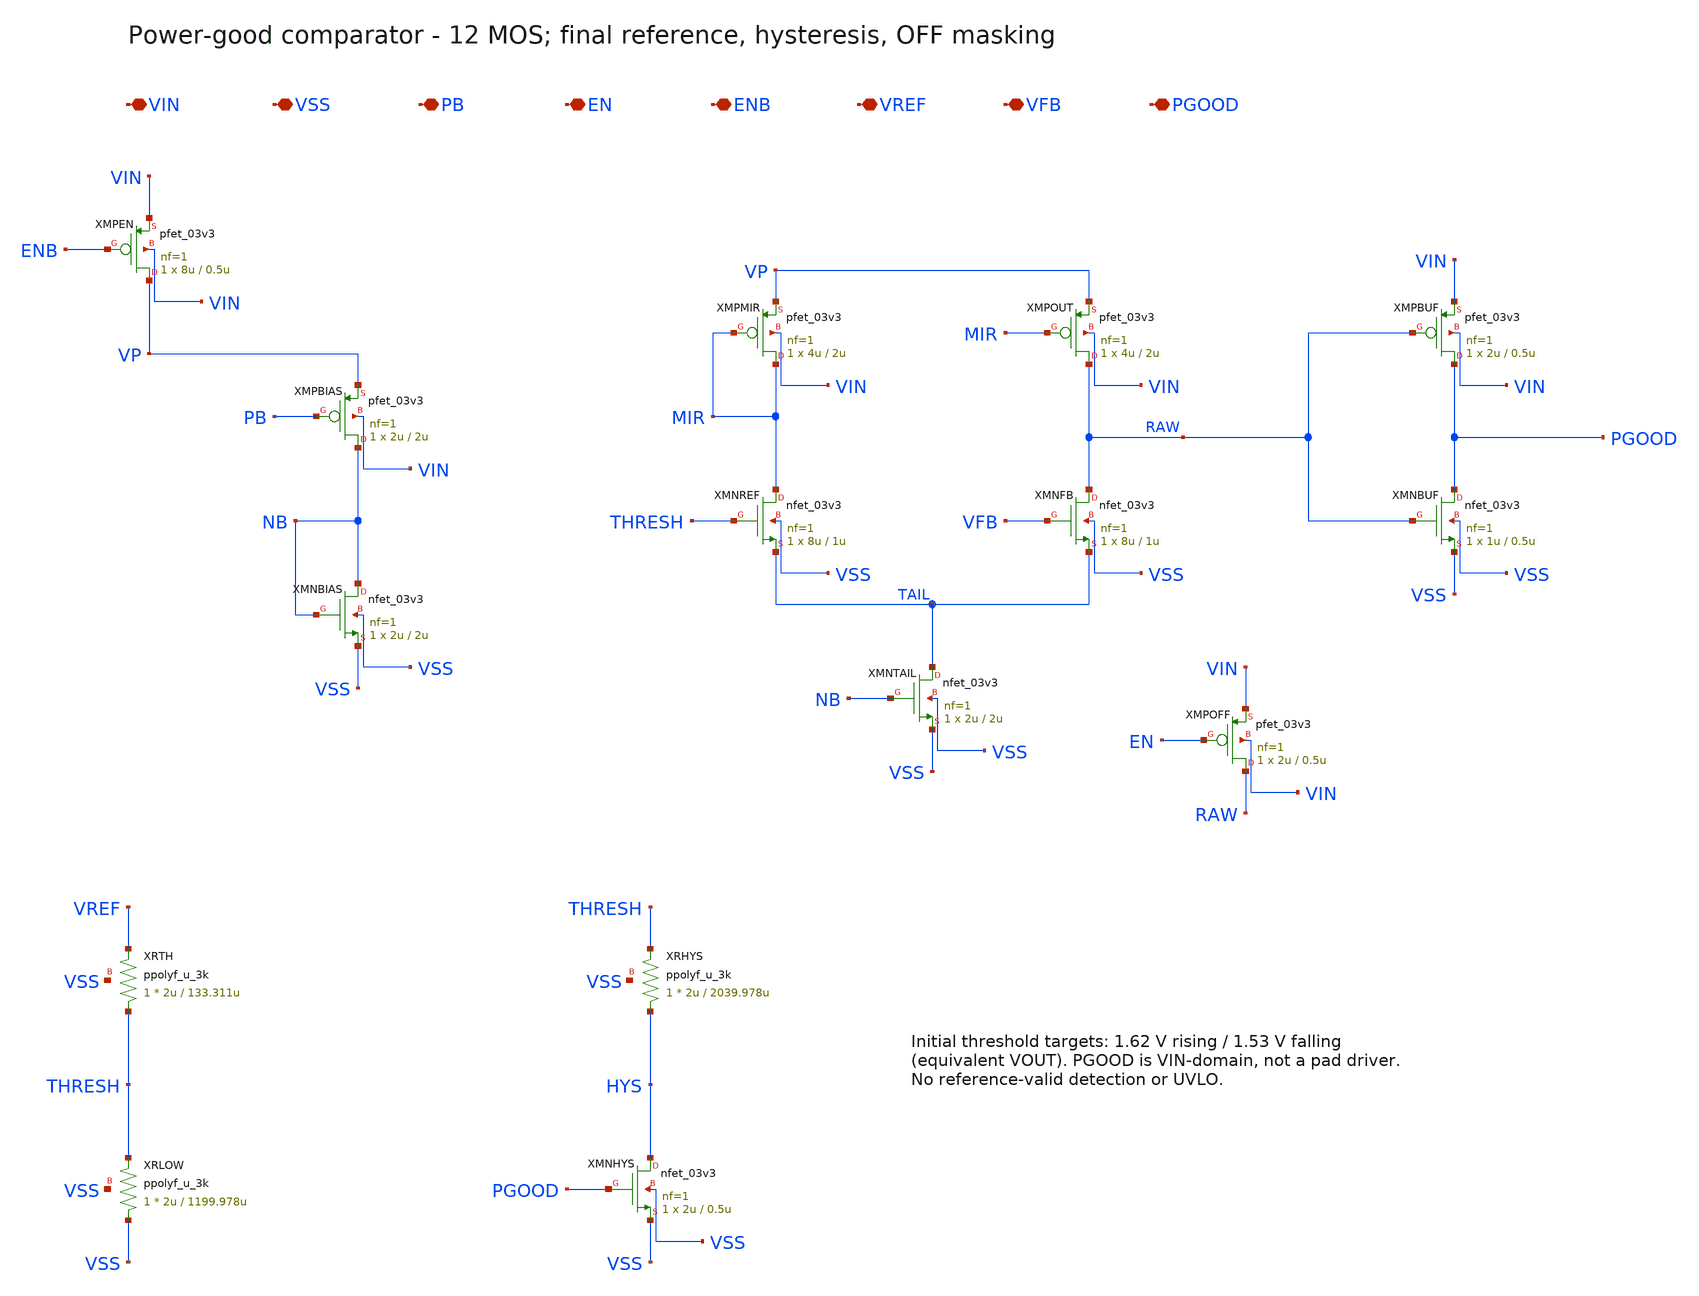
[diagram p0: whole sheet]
** sch_path: schematics/ldo_pgood.sch
**.subckt ldo_pgood VIN VSS PB EN ENB VREF VFB PGOOD
*.iopin VIN
*.iopin VSS
*.iopin PB
*.iopin EN
*.iopin ENB
*.iopin VREF
*.iopin VFB
*.iopin PGOOD
XMPEN VP ENB VIN VIN pfet_03v3 L=0.5u W=8u nf=1 ad='int((nf+1)/2)*W/nf*0.18u' as='int((nf+2)/2)*W/nf*0.18u'
+ pd='2*int((nf+1)/2)*(W/nf+0.18u)' ps='2*int((nf+2)/2)*(W/nf+0.18u)' nrd='0.18u/W' nrs='0.18u/W' sa=0
+ sb=0 sd=0 m=1 par=1
XMPBIAS NB PB VP VIN pfet_03v3 L=2u W=2u nf=1 ad='int((nf+1)/2)*W/nf*0.18u' as='int((nf+2)/2)*W/nf*0.18u'
+ pd='2*int((nf+1)/2)*(W/nf+0.18u)' ps='2*int((nf+2)/2)*(W/nf+0.18u)' nrd='0.18u/W' nrs='0.18u/W' sa=0
+ sb=0 sd=0 m=1 par=1
XMNBIAS NB NB VSS VSS nfet_03v3 L=2u W=2u nf=1 ad='int((nf+1)/2)*W/nf*0.18u' as='int((nf+2)/2)*W/nf*0.18u'
+ pd='2*int((nf+1)/2)*(W/nf+0.18u)' ps='2*int((nf+2)/2)*(W/nf+0.18u)' nrd='0.18u/W' nrs='0.18u/W' sa=0
+ sb=0 sd=0 m=1 par=1
XMPMIR MIR MIR VP VIN pfet_03v3 L=2u W=4u nf=1 ad='int((nf+1)/2)*W/nf*0.18u' as='int((nf+2)/2)*W/nf*0.18u'
+ pd='2*int((nf+1)/2)*(W/nf+0.18u)' ps='2*int((nf+2)/2)*(W/nf+0.18u)' nrd='0.18u/W' nrs='0.18u/W' sa=0
+ sb=0 sd=0 m=1 par=1
XMPOUT RAW MIR VP VIN pfet_03v3 L=2u W=4u nf=1 ad='int((nf+1)/2)*W/nf*0.18u' as='int((nf+2)/2)*W/nf*0.18u'
+ pd='2*int((nf+1)/2)*(W/nf+0.18u)' ps='2*int((nf+2)/2)*(W/nf+0.18u)' nrd='0.18u/W' nrs='0.18u/W' sa=0
+ sb=0 sd=0 m=1 par=1
XMNREF MIR THRESH TAIL VSS nfet_03v3 L=1u W=8u nf=1 ad='int((nf+1)/2)*W/nf*0.18u' as='int((nf+2)/2)*W/nf*0.18u'
+ pd='2*int((nf+1)/2)*(W/nf+0.18u)' ps='2*int((nf+2)/2)*(W/nf+0.18u)' nrd='0.18u/W' nrs='0.18u/W' sa=0
+ sb=0 sd=0 m=1 par=1
XMNFB RAW VFB TAIL VSS nfet_03v3 L=1u W=8u nf=1 ad='int((nf+1)/2)*W/nf*0.18u' as='int((nf+2)/2)*W/nf*0.18u'
+ pd='2*int((nf+1)/2)*(W/nf+0.18u)' ps='2*int((nf+2)/2)*(W/nf+0.18u)' nrd='0.18u/W' nrs='0.18u/W' sa=0
+ sb=0 sd=0 m=1 par=1
XMNTAIL TAIL NB VSS VSS nfet_03v3 L=2u W=2u nf=1 ad='int((nf+1)/2)*W/nf*0.18u' as='int((nf+2)/2)*W/nf*0.18u'
+ pd='2*int((nf+1)/2)*(W/nf+0.18u)' ps='2*int((nf+2)/2)*(W/nf+0.18u)' nrd='0.18u/W' nrs='0.18u/W' sa=0
+ sb=0 sd=0 m=1 par=1
XMPBUF PGOOD RAW VIN VIN pfet_03v3 L=0.5u W=2u nf=1 ad='int((nf+1)/2)*W/nf*0.18u' as='int((nf+2)/2)*W/nf*0.18u'
+ pd='2*int((nf+1)/2)*(W/nf+0.18u)' ps='2*int((nf+2)/2)*(W/nf+0.18u)' nrd='0.18u/W' nrs='0.18u/W' sa=0
+ sb=0 sd=0 m=1 par=1
XMNBUF PGOOD RAW VSS VSS nfet_03v3 L=0.5u W=1u nf=1 ad='int((nf+1)/2)*W/nf*0.18u' as='int((nf+2)/2)*W/nf*0.18u'
+ pd='2*int((nf+1)/2)*(W/nf+0.18u)' ps='2*int((nf+2)/2)*(W/nf+0.18u)' nrd='0.18u/W' nrs='0.18u/W' sa=0
+ sb=0 sd=0 m=1 par=1
XMPOFF RAW EN VIN VIN pfet_03v3 L=0.5u W=2u nf=1 ad='int((nf+1)/2)*W/nf*0.18u' as='int((nf+2)/2)*W/nf*0.18u'
+ pd='2*int((nf+1)/2)*(W/nf+0.18u)' ps='2*int((nf+2)/2)*(W/nf+0.18u)' nrd='0.18u/W' nrs='0.18u/W' sa=0
+ sb=0 sd=0 m=1 par=1
XRTH THRESH VREF VSS ppolyf_u_3k r_width=2u r_length=133.311u m=1
XRLOW VSS THRESH VSS ppolyf_u_3k r_width=2u r_length=1199.978u m=1
XRHYS HYS THRESH VSS ppolyf_u_3k r_width=2u r_length=2039.978u m=1
XMNHYS HYS PGOOD VSS VSS nfet_03v3 L=0.5u W=2u nf=1 ad='int((nf+1)/2)*W/nf*0.18u' as='int((nf+2)/2)*W/nf*0.18u'
+ pd='2*int((nf+1)/2)*(W/nf+0.18u)' ps='2*int((nf+2)/2)*(W/nf+0.18u)' nrd='0.18u/W' nrs='0.18u/W' sa=0
+ sb=0 sd=0 m=1 par=1
**.ends
.end
